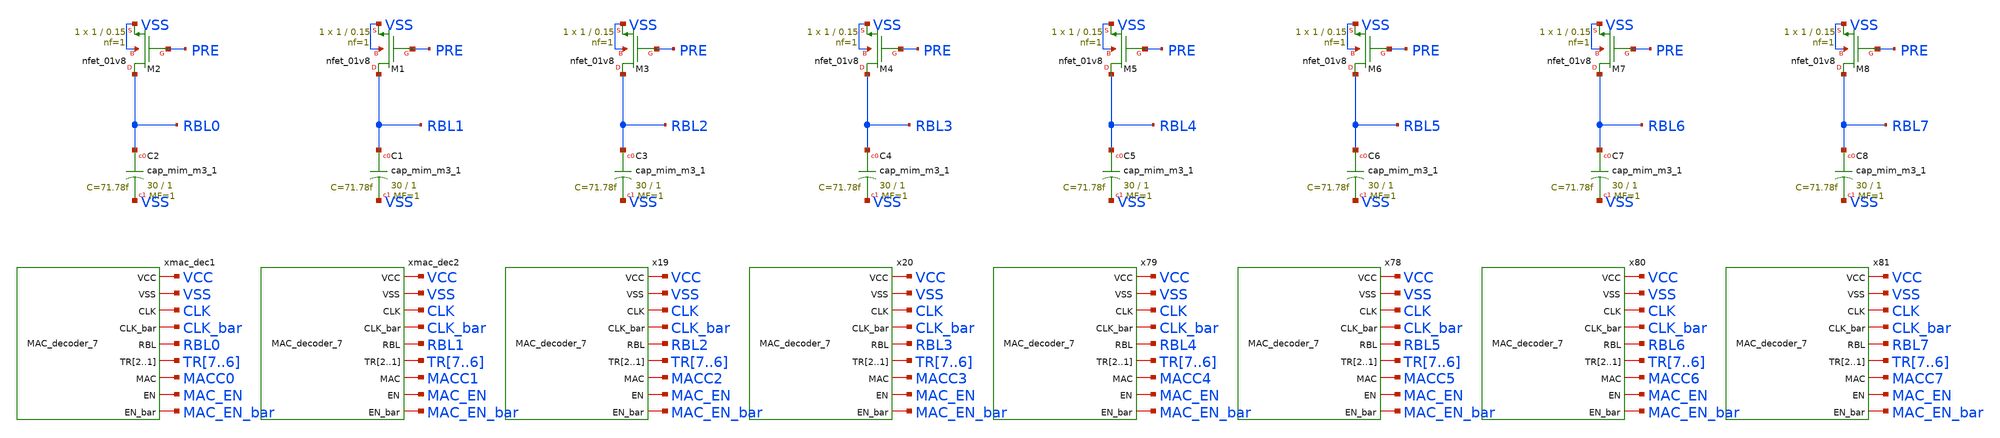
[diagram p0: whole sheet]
** sch_path: peripherals/ham-mac_decoder_7.sch
**.subckt ham-mac_decoder_7
XC3 RBL2 VSS sky130_fd_pr__cap_mim_m3_1 W=30 L=1 MF=1 m=1
XM3 RBL2 PRE VSS VSS sky130_fd_pr__nfet_01v8 L=0.15 W=1 nf=1 ad='int((1 + 1)/2) * 1 / 1 * 0.29' as='int((1 + 2)/2) * 1 / 1 * 0.29'
+ pd='2*int((1 + 1)/2) * (1 / 1 + 0.29)' ps='2*int((1 + 2)/2) * (1 / 1 + 0.29)' nrd='0.29 / 1 ' nrs='0.29 / 1 '
+ sa=0 sb=0 sd=0 mult=1 m=1
XC4 RBL3 VSS sky130_fd_pr__cap_mim_m3_1 W=30 L=1 MF=1 m=1
XM4 RBL3 PRE VSS VSS sky130_fd_pr__nfet_01v8 L=0.15 W=1 nf=1 ad='int((1 + 1)/2) * 1 / 1 * 0.29' as='int((1 + 2)/2) * 1 / 1 * 0.29'
+ pd='2*int((1 + 1)/2) * (1 / 1 + 0.29)' ps='2*int((1 + 2)/2) * (1 / 1 + 0.29)' nrd='0.29 / 1 ' nrs='0.29 / 1 '
+ sa=0 sb=0 sd=0 mult=1 m=1
xmac_dec1 VCC VSS CLK CLK_bar RBL0 TR7 TR6 MACC0 MAC_EN MAC_EN_bar MAC_decoder_7
XC2 RBL0 VSS sky130_fd_pr__cap_mim_m3_1 W=30 L=1 MF=1 m=1
XM2 RBL0 PRE VSS VSS sky130_fd_pr__nfet_01v8 L=0.15 W=1 nf=1 ad='int((1 + 1)/2) * 1 / 1 * 0.29' as='int((1 + 2)/2) * 1 / 1 * 0.29'
+ pd='2*int((1 + 1)/2) * (1 / 1 + 0.29)' ps='2*int((1 + 2)/2) * (1 / 1 + 0.29)' nrd='0.29 / 1 ' nrs='0.29 / 1 '
+ sa=0 sb=0 sd=0 mult=1 m=1
xmac_dec2 VCC VSS CLK CLK_bar RBL1 TR7 TR6 MACC1 MAC_EN MAC_EN_bar MAC_decoder_7
XC1 RBL1 VSS sky130_fd_pr__cap_mim_m3_1 W=30 L=1 MF=1 m=1
XM1 RBL1 PRE VSS VSS sky130_fd_pr__nfet_01v8 L=0.15 W=1 nf=1 ad='int((1 + 1)/2) * 1 / 1 * 0.29' as='int((1 + 2)/2) * 1 / 1 * 0.29'
+ pd='2*int((1 + 1)/2) * (1 / 1 + 0.29)' ps='2*int((1 + 2)/2) * (1 / 1 + 0.29)' nrd='0.29 / 1 ' nrs='0.29 / 1 '
+ sa=0 sb=0 sd=0 mult=1 m=1
x19 VCC VSS CLK CLK_bar RBL2 TR7 TR6 MACC2 MAC_EN MAC_EN_bar MAC_decoder_7
x20 VCC VSS CLK CLK_bar RBL3 TR7 TR6 MACC3 MAC_EN MAC_EN_bar MAC_decoder_7
XC5 RBL4 VSS sky130_fd_pr__cap_mim_m3_1 W=30 L=1 MF=1 m=1
XM5 RBL4 PRE VSS VSS sky130_fd_pr__nfet_01v8 L=0.15 W=1 nf=1 ad='int((1 + 1)/2) * 1 / 1 * 0.29' as='int((1 + 2)/2) * 1 / 1 * 0.29'
+ pd='2*int((1 + 1)/2) * (1 / 1 + 0.29)' ps='2*int((1 + 2)/2) * (1 / 1 + 0.29)' nrd='0.29 / 1 ' nrs='0.29 / 1 '
+ sa=0 sb=0 sd=0 mult=1 m=1
XC6 RBL5 VSS sky130_fd_pr__cap_mim_m3_1 W=30 L=1 MF=1 m=1
XM6 RBL5 PRE VSS VSS sky130_fd_pr__nfet_01v8 L=0.15 W=1 nf=1 ad='int((1 + 1)/2) * 1 / 1 * 0.29' as='int((1 + 2)/2) * 1 / 1 * 0.29'
+ pd='2*int((1 + 1)/2) * (1 / 1 + 0.29)' ps='2*int((1 + 2)/2) * (1 / 1 + 0.29)' nrd='0.29 / 1 ' nrs='0.29 / 1 '
+ sa=0 sb=0 sd=0 mult=1 m=1
XC7 RBL6 VSS sky130_fd_pr__cap_mim_m3_1 W=30 L=1 MF=1 m=1
XM7 RBL6 PRE VSS VSS sky130_fd_pr__nfet_01v8 L=0.15 W=1 nf=1 ad='int((1 + 1)/2) * 1 / 1 * 0.29' as='int((1 + 2)/2) * 1 / 1 * 0.29'
+ pd='2*int((1 + 1)/2) * (1 / 1 + 0.29)' ps='2*int((1 + 2)/2) * (1 / 1 + 0.29)' nrd='0.29 / 1 ' nrs='0.29 / 1 '
+ sa=0 sb=0 sd=0 mult=1 m=1
XC8 RBL7 VSS sky130_fd_pr__cap_mim_m3_1 W=30 L=1 MF=1 m=1
XM8 RBL7 PRE VSS VSS sky130_fd_pr__nfet_01v8 L=0.15 W=1 nf=1 ad='int((1 + 1)/2) * 1 / 1 * 0.29' as='int((1 + 2)/2) * 1 / 1 * 0.29'
+ pd='2*int((1 + 1)/2) * (1 / 1 + 0.29)' ps='2*int((1 + 2)/2) * (1 / 1 + 0.29)' nrd='0.29 / 1 ' nrs='0.29 / 1 '
+ sa=0 sb=0 sd=0 mult=1 m=1
x78 VCC VSS CLK CLK_bar RBL5 TR7 TR6 MACC5 MAC_EN MAC_EN_bar MAC_decoder_7
x79 VCC VSS CLK CLK_bar RBL4 TR7 TR6 MACC4 MAC_EN MAC_EN_bar MAC_decoder_7
x80 VCC VSS CLK CLK_bar RBL6 TR7 TR6 MACC6 MAC_EN MAC_EN_bar MAC_decoder_7
x81 VCC VSS CLK CLK_bar RBL7 TR7 TR6 MACC7 MAC_EN MAC_EN_bar MAC_decoder_7
**.ends
.end
